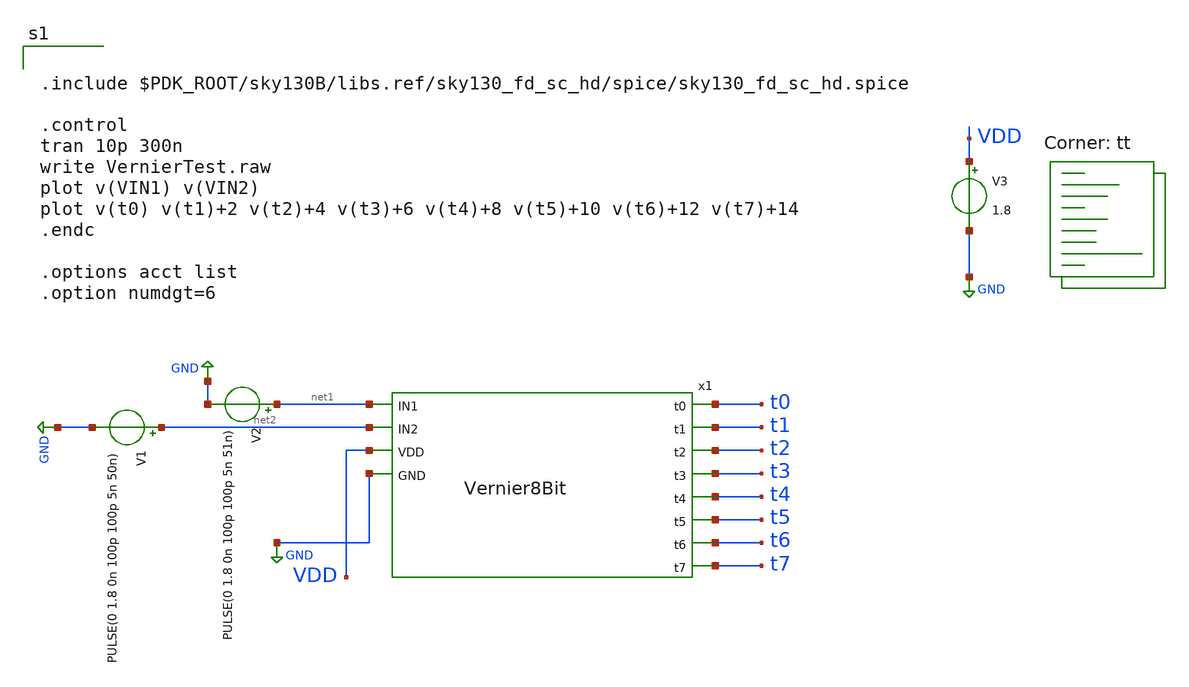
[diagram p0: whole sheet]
** sch_path: xschem/projects/8BitTest.sch
**.subckt 8BitTest
V1 net2 GND PULSE(0 1.8 0n 100p 100p 5n 50n)
V2 net1 GND PULSE(0 1.8 0n 100p 100p 5n 51n)
V3 VDD GND 1.8
x1 t0 t1 t2 t3 t4 t5 t6 t7 net1 net2 VDD GND Vernier8Bit
**** begin user architecture code


.include $PDK_ROOT/sky130B/libs.ref/sky130_fd_sc_hd/spice/sky130_fd_sc_hd.spice

.control
tran 10p 300n
write VernierTest.raw
plot v(VIN1) v(VIN2)
plot v(t0) v(t1)+2 v(t2)+4 v(t3)+6 v(t4)+8 v(t5)+10 v(t6)+12 v(t7)+14
.endc

.options acct list
.option numdgt=6


.lib $::SKYWATER_MODELS/sky130.lib.spice tt
**** end user architecture code
**.ends

* expanding   symbol:  Vernier8Bit.sym # of pins=12
** sym_path: xschem/projects/Vernier8Bit.sym
** sch_path: xschem/projects/Vernier8Bit.sch
.subckt Vernier8Bit t0 t1 t2 t3 t4 t5 t6 t7 IN1 IN2 VDD GND
*.ipin VDD
*.ipin GND
*.ipin IN1
*.ipin IN2
*.opin t0
*.opin t7
*.opin t1
*.opin t2
*.opin t3
*.opin t4
*.opin t5
*.opin t6
x16 t0 IN1 net1 IN2 VDD GND VernierSymbol
x1 t1 t0 net2 net1 VDD GND VernierSymbol
x2 t2 t1 net3 net2 VDD GND VernierSymbol
x3 t3 t2 net7 net3 VDD GND VernierSymbol
x4 t4 t3 net4 net7 VDD GND VernierSymbol
x7 t5 t4 net5 net4 VDD GND VernierSymbol
x8 t6 t5 net6 net5 VDD GND VernierSymbol
x9 t7 t6 net8 net6 VDD GND VernierSymbol
* noconn #net8
.ends


* expanding   symbol:  VernierSymbol.sym # of pins=6
** sym_path: xschem/projects/VernierSymbol.sym
** sch_path: xschem/projects/VernierSymbol.sch
.subckt VernierSymbol OUT1 IN1 OUT2 IN2 VDD GND
*.ipin VDD
*.ipin GND
*.ipin IN1
*.ipin IN2
*.opin OUT1
*.opin OUT2
x2 net8 OUT2 0 0 VDD VDD OUT1 sky130_fd_sc_hd__dlxtp_1
x10 net5 GND GND VDD VDD net7 sky130_fd_sc_hd__buf_1
x11 net4 GND GND VDD VDD net5 sky130_fd_sc_hd__buf_1
x12 IN2 GND GND VDD VDD net4 sky130_fd_sc_hd__buf_1
x6 net3 GND GND VDD VDD net6 sky130_fd_sc_hd__buf_1
x7 net2 GND GND VDD VDD net3 sky130_fd_sc_hd__buf_1
x8 net1 GND GND VDD VDD net2 sky130_fd_sc_hd__buf_1
x9 IN1 GND GND VDD VDD net1 sky130_fd_sc_hd__buf_1
x5 net6 GND GND VDD VDD net8 sky130_fd_sc_hd__buf_1
x13 net7 GND GND VDD VDD OUT2 sky130_fd_sc_hd__buf_1
.ends

.GLOBAL GND
.end
